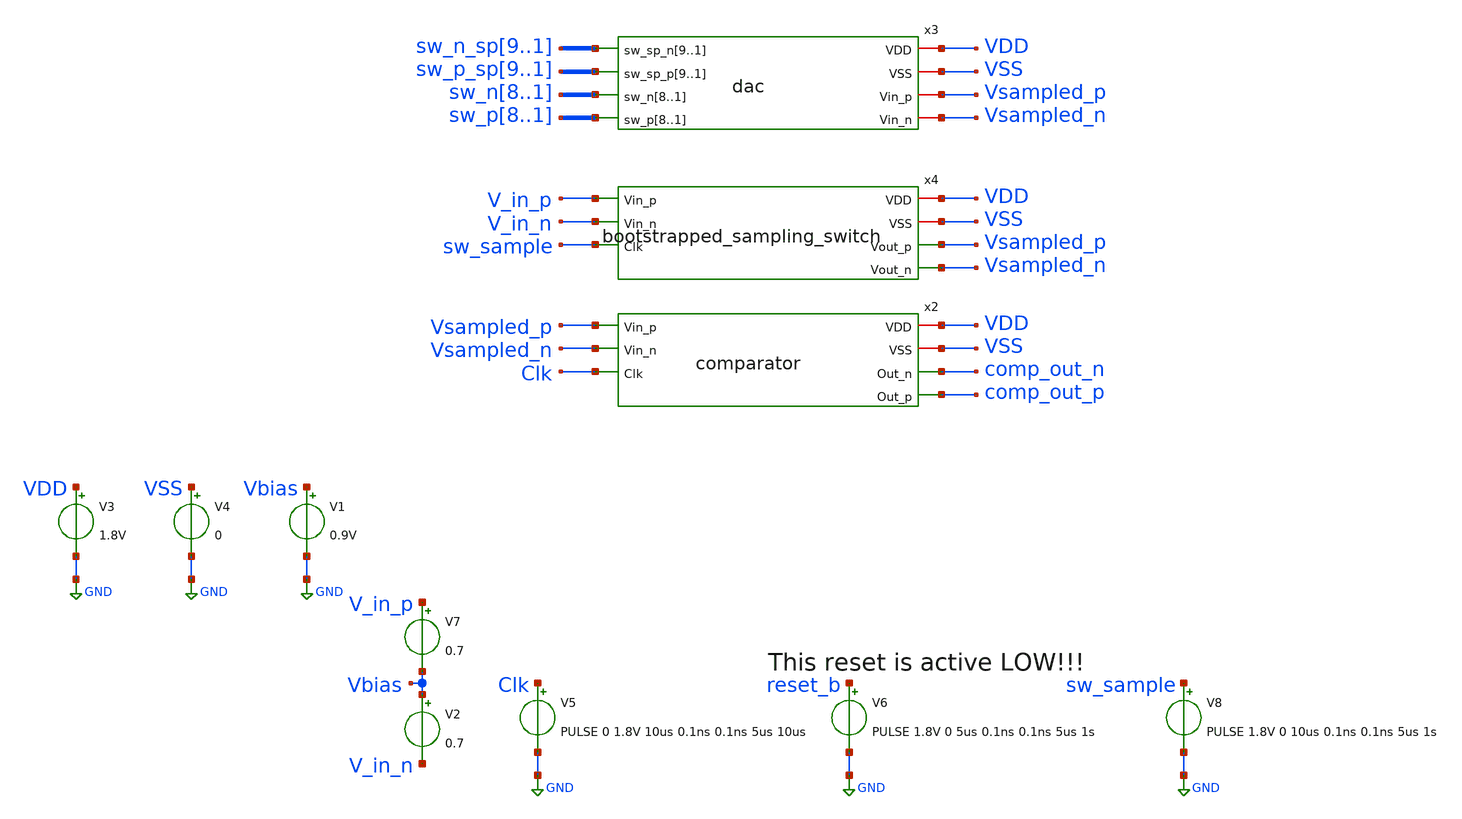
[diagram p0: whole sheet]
** sch_path: xschem/tests/sar_adc/comparator_dac_test.sch
**.subckt comparator_dac_test
V3 VDD GND 1.8V
V4 VSS GND 0
V2 Vbias V_in_n 0.7
V5 Clk GND PULSE 0 1.8V 10us 0.1ns 0.1ns 5us 10us
V6 reset_b GND PULSE 1.8V 0 5us 0.1ns 0.1ns 5us 1s
V1 Vbias GND 0.9V
V7 V_in_p Vbias 0.7
x2 VDD VSS Vsampled_p comp_out_n Vsampled_n comp_out_p Clk comparator
x4 VDD V_in_p VSS V_in_n sw_sample Vsampled_p Vsampled_n bootstrapped_sampling_switch
V8 sw_sample GND PULSE 1.8V 0 10us 0.1ns 0.1ns 5us 1s
x3 sw_n_sp9 sw_n_sp8 sw_n_sp7 sw_n_sp6 sw_n_sp5 sw_n_sp4 sw_n_sp3 sw_n_sp2 sw_n_sp1 VDD sw_p_sp9
+ sw_p_sp8 sw_p_sp7 sw_p_sp6 sw_p_sp5 sw_p_sp4 sw_p_sp3 sw_p_sp2 sw_p_sp1 VSS sw_n8 sw_n7 sw_n6 sw_n5 sw_n4
+ sw_n3 sw_n2 sw_n1 Vsampled_p sw_p8 sw_p7 sw_p6 sw_p5 sw_p4 sw_p3 sw_p2 sw_p1 Vsampled_n dac
**** begin user architecture code
 .lib $::SKYWATER_MODELS/sky130.lib.spice tt
.include $::SKYWATER_STDCELLS/sky130_fd_sc_hd.spice


.options acct list
.temp 25
*vvcc VDD 0 dc 1.8
*vvss VSS 0 0

v_sp_n1 sw_sp_n1 gnd 1.8V
v_sp_n2 sw_sp_n2 gnd 1.8V
v_sp_n3 sw_sp_n3 gnd 1.8V
v_sp_n4 sw_sp_n4 gnd 1.8V
v_sp_n5 sw_sp_n5 gnd 1.8V
v_sp_n6 sw_sp_n6 gnd 1.8V
v_sp_n7 sw_sp_n7 gnd 1.8V
v_sp_n8 sw_sp_n8 gnd 1.8V
v_sp_n9 sw_sp_n9 gnd 1.8V

v_n1 sw_n1 gnd 0
v_n2 sw_n2 gnd 0
v_n3 sw_n3 gnd 0
v_n4 sw_n4 gnd 0
v_n5 sw_n5 gnd 0
v_n6 sw_n6 gnd 0
v_n7 sw_n7 gnd 0
v_n8 sw_n8 gnd 0

v_sp_p1 sw_sp_p1 gnd 1.8V
v_sp_p2 sw_sp_p2 gnd 1.8V
v_sp_p3 sw_sp_p3 gnd 1.8V
v_sp_p4 sw_sp_p4 gnd 1.8V
v_sp_p5 sw_sp_p5 gnd 1.8V
v_sp_p6 sw_sp_p6 gnd 1.8V
v_sp_p7 sw_sp_p7 gnd 1.8V
v_sp_p8 sw_sp_p8 gnd 1.8V
v_sp_p9 sw_sp_p9 gnd 1.8V

v_p1 sw_p1 gnd 0
v_p2 sw_p2 gnd 0
v_p3 sw_p3 gnd 0
v_p4 sw_p4 gnd 0
v_p5 sw_p5 gnd 0
v_p6 sw_p6 gnd 0
v_p7 sw_p7 gnd 0
v_p8 sw_p8 gnd 0

.control
tran 0.01u 400u
*plot RST_PLS clk+2 Pulse+4
write comparator_dac_test.raw
.endc


**** end user architecture code
**.ends
.GLOBAL GND
.end
